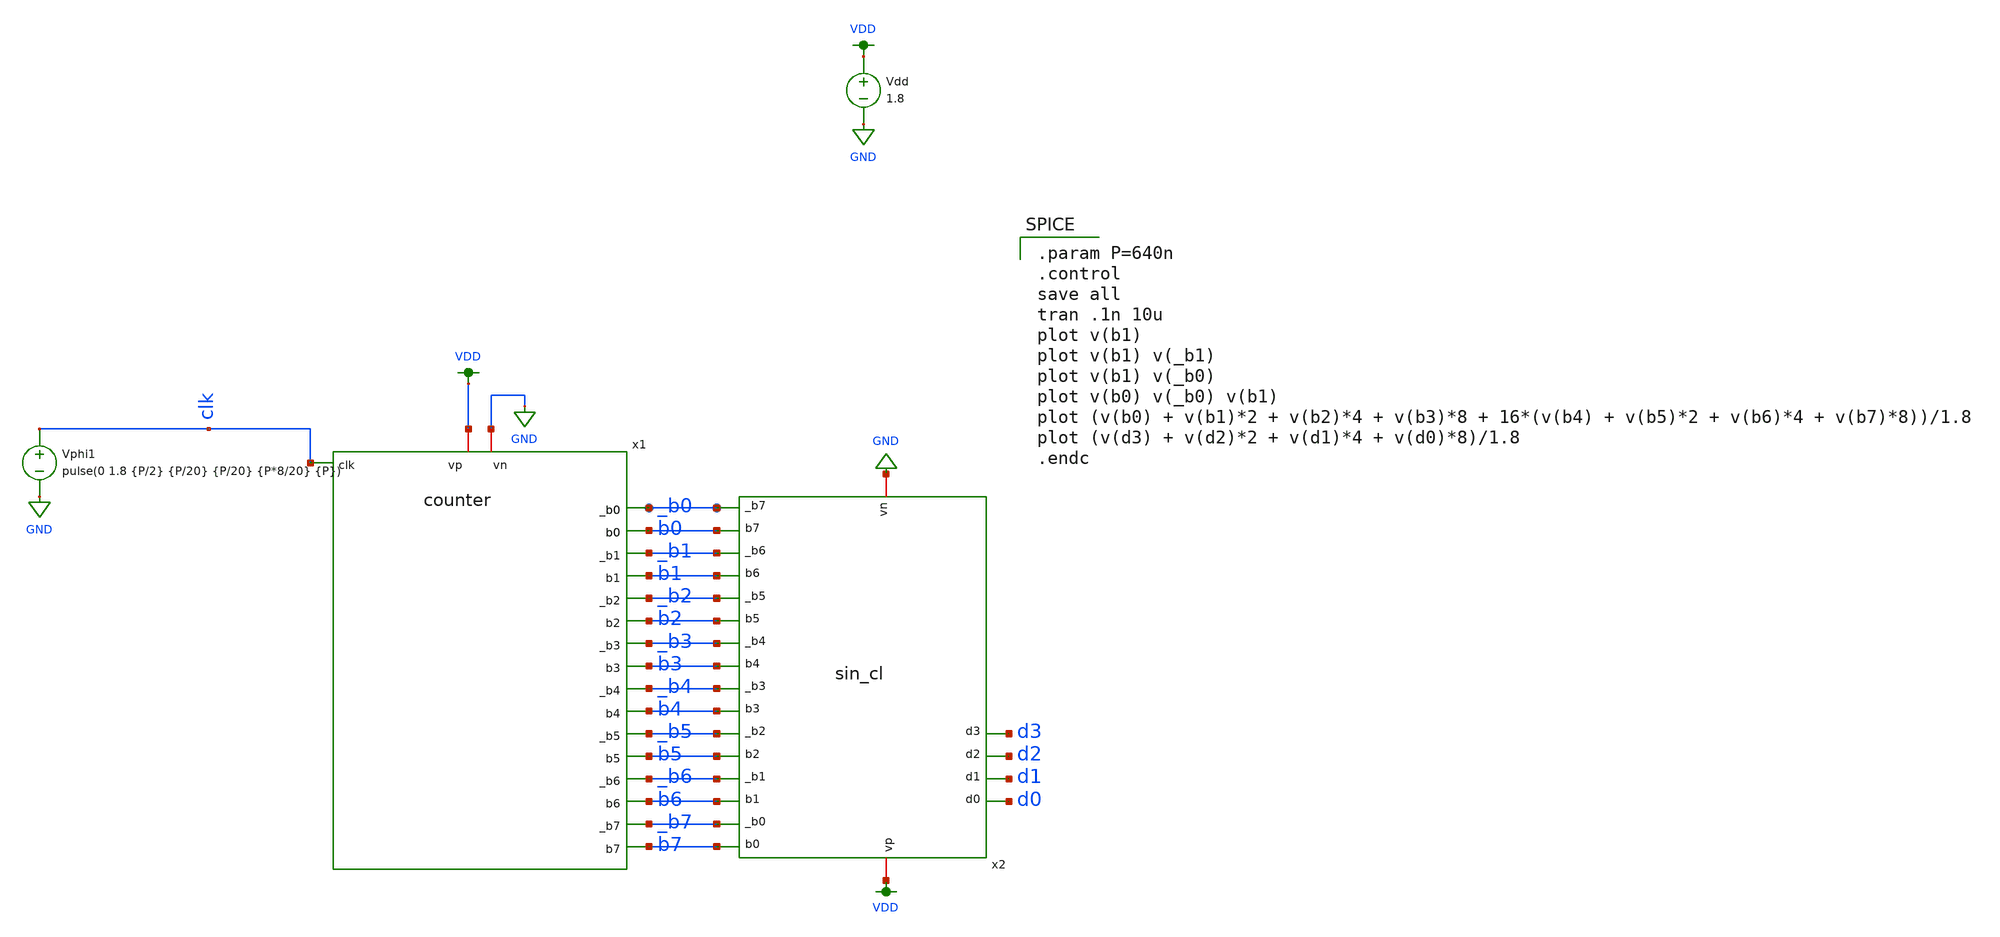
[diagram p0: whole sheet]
** sch_path: xschem/counter_testbench.sch
**.subckt counter_testbench
Vdd VDD GND 1.8
x1 VDD GND clk _b1 b1 _b2 b2 _b3 b3 _b0 b0 _b5 b5 _b6 b6 _b7 b7 _b4 b4 counter
x2 b6 _b6 b5 _b5 b4 _b4 b3 VDD _b3 GND b2 _b2 b1 _b1 d0 b7 b0 _b7 _b0 d1 d2 d3 sin_cl
Vphi1 clk GND pulse(0 1.8 {P/2} {P/20} {P/20} {P*8/20} {P})
**** begin user architecture code

.option wnflag=1
.param MC_SWITCH=0.0
.lib ~/skywater/skywater-pdk/libraries/sky130_fd_pr_ngspice/latest/models/sky130.lib.spice tt


.param P=640n
.control
save all
tran .1n 10u
plot v(b1)
plot v(b1) v(_b1)
plot v(b1) v(_b0)
plot v(b0) v(_b0) v(b1)
plot (v(b0) + v(b1)*2 + v(b2)*4 + v(b3)*8 + 16*(v(b4) + v(b5)*2 + v(b6)*4 + v(b7)*8))/1.8
plot (v(d3) + v(d2)*2 + v(d1)*4 + v(d0)*8)/1.8
.endc

**** end user architecture code
**.ends

* expanding   symbol:  /home/madvlsi/dev/git/magic-dds/xschem/logic_gates/counter.sym # of pins=19
** sym_path: xschem/logic_gates/counter.sym
** sch_path: xschem/logic_gates/counter.sch
.subckt counter vp vn clk _b1 b1 _b2 b2 _b3 b3 _b0 b0 _b5 b5 _b6 b6 _b7 b7 _b4 b4
*.iopin vp
*.iopin vn
*.ipin clk
*.opin b0
*.opin _b0
*.opin b1
*.opin _b1
*.opin b2
*.opin _b2
*.opin b3
*.opin _b3
*.opin b4
*.opin _b4
*.opin b5
*.opin _b5
*.opin b6
*.opin _b6
*.opin b7
*.opin _b7
X1 net2 net1 _b0 b0 clk vp vn dflipflop
x3 vp net2 b0 vn inverter
x2 vp net1 _b0 vn inverter
X4 net4 net3 _b1 b1 _b0 vp vn dflipflop
x5 vp net4 b1 vn inverter
x6 vp net3 _b1 vn inverter
X7 net6 net5 _b2 b2 _b1 vp vn dflipflop
x8 vp net6 b2 vn inverter
x9 vp net5 _b2 vn inverter
X10 net8 net7 _b3 b3 _b2 vp vn dflipflop
x11 vp net8 b3 vn inverter
x12 vp net7 _b3 vn inverter
X13 net10 net9 _b4 b4 _b3 vp vn dflipflop
x14 vp net10 b4 vn inverter
x15 vp net9 _b4 vn inverter
X16 net12 net11 _b5 b5 _b4 vp vn dflipflop
x17 vp net12 b5 vn inverter
x18 vp net11 _b5 vn inverter
X19 net14 net13 _b6 b6 _b5 vp vn dflipflop
x20 vp net14 b6 vn inverter
x21 vp net13 _b6 vn inverter
X22 net16 net15 _b7 b7 _b6 vp vn dflipflop
x23 vp net16 b7 vn inverter
x24 vp net15 _b7 vn inverter
.ends


* expanding   symbol:  /home/madvlsi/dev/git/magic-dds/xschem/sin_cl.sym # of pins=22
** sym_path: xschem/sin_cl.sym
** sch_path: xschem/sin_cl.sch
.subckt sin_cl b1 _b1 b2 _b2 b3 _b3 b4 vp _b4 vn b5 _b5 b6 _b6 d0 b0 b7 _b0 _b7 d1 d2 d3
*.ipin _b0
*.ipin b1
*.ipin _b1
*.ipin b2
*.ipin _b2
*.ipin b3
*.ipin _b3
*.ipin b4
*.ipin _b4
*.ipin b5
*.ipin _b5
*.ipin b6
*.ipin _b6
*.ipin b7
*.ipin _b7
*.ipin b0
*.opin d0
*.opin d1
*.opin d2
*.opin d3
*.iopin vp
*.iopin vn
x1 vp b0 d0 vn inverter
x2 vp _b0 net2 d1 b0 net1 vn xnor
x3 vp net2 net1 vn inverter
x4 vn b1 _b2 net3 vp nand
x5 vn _b1 b2 net4 vp nand
x6 vn _b1 b3 net5 vp b4 nand3
x7 vn b2 _b3 net6 vp _b4 nand3
x8 vn _b1 b4 net7 vp b5 b6 nand4
x9 vn net3 net4 net2 vp net5 net6 net7 nand5
x10 vp _b0 net9 d2 b0 net8 vn xnor
x11 vp net9 net8 vn inverter
x12 vn b1 _b3 net13 vp b4 nand3
x13 vn _b1 b2 net10 vp b4 nand3
x14 vn _b1 b2 net11 vp b5 nand3
x15 vn _b3 b4 net12 vp b5 nand3
x16 vn b1 _b2 net16 vp _b4 nand3
x17 vn b1 _b2 net15 vp _b4 nand3
x18 vn b3 _b4 net14 vp _b5 nand3
x19 vn b3 _b4 net17 vp _b6 nand3
x20 vn net13 net10 net39 vp net11 net12 nand4
x21 vn net16 net15 net40 vp net14 net17 nand4
x22 vp net40 net19 vn inverter
x23 vp net39 net18 vn inverter
x24 vn net18 net19 net9 vp nand
x25 vn _b1 b2 net22 vp b3 nand3
x26 vn b1 b2 net21 vp _b3 b4 nand4
x27 vn b1 _b2 net20 vp b3 b4 nand4
x28 vn b1 b4 net23 vp _b5 _b6 nand4
x29 vn b2 b3 net24 vp _b4 b5 b6 nand5
x30 vn b2 _b3 net27 vp b4 b5 b6 nand5
x31 vn _b2 b3 net26 vp b4 b5 b6 nand5
x32 vn b1 _b2 net25 vp _b3 _b6 nand4
x33 vn b1 _b2 net28 vp _b3 _b4 nand4
x34 vn b1 _b3 net29 vp _b5 _b6 nand4
x35 vn _b1 b2 net32 vp _b4 _b5 nand4
x36 vn _b1 b3 net31 vp _b4 _b5 nand4
x37 vn _b1 b3 net30 vp _b4 _b6 nand4
x38 vn _b2 _b3 net33 vp b4 b5 nand4
x39 vn _b2 _b3 net34 vp _b4 b5 b6 nand5
x40 vn net22 net21 net41 vp net20 net23 net24 nand5
x41 vn net27 net26 net42 vp net25 net28 net29 nand5
x42 vn net32 net31 net43 vp net30 net33 net34 nand5
x43 vp net41 net35 vn inverter
x44 vp net42 net44 vn inverter
x45 vp net43 net36 vn inverter
x46 vn net35 net44 net37 vp net36 nand3
x47 vp _b0 net37 d3 b0 net38 vn xnor
x48 net45 net37 net38 vn inverter
.ends


* expanding   symbol:  /home/madvlsi/dev/git/magic-dds/xschem/logic_gates/dflipflop.sym # of pins=7
** sym_path: xschem/logic_gates/dflipflop.sym
** sch_path: xschem/logic_gates/dflipflop.sch
.subckt dflipflop q_bar q d d_bar clk vp vn
*.opin q
*.opin q_bar
*.iopin vp
*.iopin vn
*.ipin d_bar
*.ipin d
*.ipin clk
XM8 vp net2 net3 vp sky130_fd_pr__pfet_01v8 L=0.15 W=1 nf=1 ad='int((nf+1)/2) * W/nf * 0.29' as='int((nf+2)/2) * W/nf * 0.29'
+ pd='2*int((nf+1)/2) * (W/nf + 0.29)' ps='2*int((nf+2)/2) * (W/nf + 0.29)' nrd='0.29 / W' nrs='0.29 / W'
+ sa=0 sb=0 sd=0 mult=1 m=1
XM9 vp net3 net2 vp sky130_fd_pr__pfet_01v8 L=0.15 W=1 nf=1 ad='int((nf+1)/2) * W/nf * 0.29' as='int((nf+2)/2) * W/nf * 0.29'
+ pd='2*int((nf+1)/2) * (W/nf + 0.29)' ps='2*int((nf+2)/2) * (W/nf + 0.29)' nrd='0.29 / W' nrs='0.29 / W'
+ sa=0 sb=0 sd=0 mult=1 m=1
XM5 net1 clk vn vn sky130_fd_pr__nfet_01v8 L=0.15 W=1 nf=1 ad='int((nf+1)/2) * W/nf * 0.29' as='int((nf+2)/2) * W/nf * 0.29'
+ pd='2*int((nf+1)/2) * (W/nf + 0.29)' ps='2*int((nf+2)/2) * (W/nf + 0.29)' nrd='0.29 / W' nrs='0.29 / W'
+ sa=0 sb=0 sd=0 mult=1 m=1
XM6 net3 net2 net1 vn sky130_fd_pr__nfet_01v8 L=0.15 W=1 nf=1 ad='int((nf+1)/2) * W/nf * 0.29' as='int((nf+2)/2) * W/nf * 0.29'
+ pd='2*int((nf+1)/2) * (W/nf + 0.29)' ps='2*int((nf+2)/2) * (W/nf + 0.29)' nrd='0.29 / W' nrs='0.29 / W'
+ sa=0 sb=0 sd=0 mult=1 m=1
XM7 net2 net3 net1 vn sky130_fd_pr__nfet_01v8 L=0.15 W=1 nf=1 ad='int((nf+1)/2) * W/nf * 0.29' as='int((nf+2)/2) * W/nf * 0.29'
+ pd='2*int((nf+1)/2) * (W/nf + 0.29)' ps='2*int((nf+2)/2) * (W/nf + 0.29)' nrd='0.29 / W' nrs='0.29 / W'
+ sa=0 sb=0 sd=0 mult=1 m=1
XM13 vn q q_bar vn sky130_fd_pr__nfet_01v8 L=0.15 W=1 nf=1 ad='int((nf+1)/2) * W/nf * 0.29' as='int((nf+2)/2) * W/nf * 0.29'
+ pd='2*int((nf+1)/2) * (W/nf + 0.29)' ps='2*int((nf+2)/2) * (W/nf + 0.29)' nrd='0.29 / W' nrs='0.29 / W'
+ sa=0 sb=0 sd=0 mult=1 m=1
XM3 q clk net2 vn sky130_fd_pr__nfet_01v8 L=0.30 W=1 nf=1 ad='int((nf+1)/2) * W/nf * 0.29' as='int((nf+2)/2) * W/nf * 0.29'
+ pd='2*int((nf+1)/2) * (W/nf + 0.29)' ps='2*int((nf+2)/2) * (W/nf + 0.29)' nrd='0.29 / W' nrs='0.29 / W'
+ sa=0 sb=0 sd=0 mult=1 m=1
XM4 q_bar clk net3 vn sky130_fd_pr__nfet_01v8 L=0.30 W=1 nf=1 ad='int((nf+1)/2) * W/nf * 0.29' as='int((nf+2)/2) * W/nf * 0.29'
+ pd='2*int((nf+1)/2) * (W/nf + 0.29)' ps='2*int((nf+2)/2) * (W/nf + 0.29)' nrd='0.29 / W' nrs='0.29 / W'
+ sa=0 sb=0 sd=0 mult=1 m=1
XM14 vn q_bar q vn sky130_fd_pr__nfet_01v8 L=0.15 W=1 nf=1 ad='int((nf+1)/2) * W/nf * 0.29' as='int((nf+2)/2) * W/nf * 0.29'
+ pd='2*int((nf+1)/2) * (W/nf + 0.29)' ps='2*int((nf+2)/2) * (W/nf + 0.29)' nrd='0.29 / W' nrs='0.29 / W'
+ sa=0 sb=0 sd=0 mult=1 m=1
XM10 net4 clk vp vp sky130_fd_pr__pfet_01v8 L=0.15 W=1 nf=1 ad='int((nf+1)/2) * W/nf * 0.29' as='int((nf+2)/2) * W/nf * 0.29'
+ pd='2*int((nf+1)/2) * (W/nf + 0.29)' ps='2*int((nf+2)/2) * (W/nf + 0.29)' nrd='0.29 / W' nrs='0.29 / W'
+ sa=0 sb=0 sd=0 mult=1 m=1
XM11 q_bar q net4 vp sky130_fd_pr__pfet_01v8 L=0.15 W=1 nf=1 ad='int((nf+1)/2) * W/nf * 0.29' as='int((nf+2)/2) * W/nf * 0.29'
+ pd='2*int((nf+1)/2) * (W/nf + 0.29)' ps='2*int((nf+2)/2) * (W/nf + 0.29)' nrd='0.29 / W' nrs='0.29 / W'
+ sa=0 sb=0 sd=0 mult=1 m=1
XM12 q q_bar net4 vp sky130_fd_pr__pfet_01v8 L=0.15 W=1 nf=1 ad='int((nf+1)/2) * W/nf * 0.29' as='int((nf+2)/2) * W/nf * 0.29'
+ pd='2*int((nf+1)/2) * (W/nf + 0.29)' ps='2*int((nf+2)/2) * (W/nf + 0.29)' nrd='0.29 / W' nrs='0.29 / W'
+ sa=0 sb=0 sd=0 mult=1 m=1
XM15 net1 clk vn vn sky130_fd_pr__nfet_01v8 L=0.15 W=1 nf=1 ad='int((nf+1)/2) * W/nf * 0.29' as='int((nf+2)/2) * W/nf * 0.29'
+ pd='2*int((nf+1)/2) * (W/nf + 0.29)' ps='2*int((nf+2)/2) * (W/nf + 0.29)' nrd='0.29 / W' nrs='0.29 / W'
+ sa=0 sb=0 sd=0 mult=1 m=1
XM16 net4 clk vp vp sky130_fd_pr__pfet_01v8 L=0.15 W=1 nf=1 ad='int((nf+1)/2) * W/nf * 0.29' as='int((nf+2)/2) * W/nf * 0.29'
+ pd='2*int((nf+1)/2) * (W/nf + 0.29)' ps='2*int((nf+2)/2) * (W/nf + 0.29)' nrd='0.29 / W' nrs='0.29 / W'
+ sa=0 sb=0 sd=0 mult=1 m=1
XM1 net2 clk d vp sky130_fd_pr__pfet_01v8 L=0.30 W=1 nf=1 ad='int((nf+1)/2) * W/nf * 0.29' as='int((nf+2)/2) * W/nf * 0.29'
+ pd='2*int((nf+1)/2) * (W/nf + 0.29)' ps='2*int((nf+2)/2) * (W/nf + 0.29)' nrd='0.29 / W' nrs='0.29 / W'
+ sa=0 sb=0 sd=0 mult=1 m=1
XM2 net3 clk d_bar vp sky130_fd_pr__pfet_01v8 L=0.30 W=1 nf=1 ad='int((nf+1)/2) * W/nf * 0.29' as='int((nf+2)/2) * W/nf * 0.29'
+ pd='2*int((nf+1)/2) * (W/nf + 0.29)' ps='2*int((nf+2)/2) * (W/nf + 0.29)' nrd='0.29 / W' nrs='0.29 / W'
+ sa=0 sb=0 sd=0 mult=1 m=1
.ends


* expanding   symbol:  /home/madvlsi/dev/git/magic-dds/xschem/other_project_files/inverter.sym # of
*+ pins=4
** sym_path: xschem/other_project_files/inverter.sym
** sch_path: xschem/other_project_files/inverter.sch
.subckt inverter VP A Y VN
*.iopin VP
*.iopin VN
*.ipin A
*.opin Y
XM1 Y A VN VN sky130_fd_pr__nfet_01v8 L=0.15 W=1 nf=1 ad='int((nf+1)/2) * W/nf * 0.29' as='int((nf+2)/2) * W/nf * 0.29'
+ pd='2*int((nf+1)/2) * (W/nf + 0.29)' ps='2*int((nf+2)/2) * (W/nf + 0.29)' nrd='0.29 / W' nrs='0.29 / W'
+ sa=0 sb=0 sd=0 mult=1 m=1
XM2 Y A VP VP sky130_fd_pr__pfet_01v8 L=0.15 W=4 nf=1 ad='int((nf+1)/2) * W/nf * 0.29' as='int((nf+2)/2) * W/nf * 0.29'
+ pd='2*int((nf+1)/2) * (W/nf + 0.29)' ps='2*int((nf+2)/2) * (W/nf + 0.29)' nrd='0.29 / W' nrs='0.29 / W'
+ sa=0 sb=0 sd=0 mult=1 m=1
.ends


* expanding   symbol:  /home/madvlsi/dev/git/magic-dds/xschem/logic_gates/xnor.sym # of pins=7
** sym_path: xschem/logic_gates/xnor.sym
** sch_path: xschem/logic_gates/xnor.sch
.subckt xnor vp A B Y _A _B vn
*.iopin vp
*.iopin vn
*.ipin A
*.ipin B
*.ipin _A
*.ipin _B
*.opin Y
x1 vn A B net1 vp nand
x2 vn _A _B net2 vp nand
x3 vn net1 net2 Y vp nand
.ends


* expanding   symbol:  /home/madvlsi/dev/git/magic-dds/xschem/logic_gates/nand.sym # of pins=5
** sym_path: xschem/logic_gates/nand.sym
** sch_path: xschem/logic_gates/nand.sch
.subckt nand VN A B Y VP
*.iopin VP
*.iopin VN
*.ipin A
*.ipin B
*.opin Y
XM1 Y A net1 GND sky130_fd_pr__nfet_01v8 L=0.15 W=1 nf=1 ad='int((nf+1)/2) * W/nf * 0.29' as='int((nf+2)/2) * W/nf * 0.29'
+ pd='2*int((nf+1)/2) * (W/nf + 0.29)' ps='2*int((nf+2)/2) * (W/nf + 0.29)' nrd='0.29 / W' nrs='0.29 / W'
+ sa=0 sb=0 sd=0 mult=1 m=1
XM2 net1 B VN GND sky130_fd_pr__nfet_01v8 L=0.15 W=1 nf=1 ad='int((nf+1)/2) * W/nf * 0.29' as='int((nf+2)/2) * W/nf * 0.29'
+ pd='2*int((nf+1)/2) * (W/nf + 0.29)' ps='2*int((nf+2)/2) * (W/nf + 0.29)' nrd='0.29 / W' nrs='0.29 / W'
+ sa=0 sb=0 sd=0 mult=1 m=1
XM3 Y A VP VDD sky130_fd_pr__pfet_01v8 L=0.15 W=1 nf=1 ad='int((nf+1)/2) * W/nf * 0.29' as='int((nf+2)/2) * W/nf * 0.29'
+ pd='2*int((nf+1)/2) * (W/nf + 0.29)' ps='2*int((nf+2)/2) * (W/nf + 0.29)' nrd='0.29 / W' nrs='0.29 / W'
+ sa=0 sb=0 sd=0 mult=1 m=1
XM4 Y B VP VDD sky130_fd_pr__pfet_01v8 L=0.15 W=1 nf=1 ad='int((nf+1)/2) * W/nf * 0.29' as='int((nf+2)/2) * W/nf * 0.29'
+ pd='2*int((nf+1)/2) * (W/nf + 0.29)' ps='2*int((nf+2)/2) * (W/nf + 0.29)' nrd='0.29 / W' nrs='0.29 / W'
+ sa=0 sb=0 sd=0 mult=1 m=1
.ends


* expanding   symbol:  /home/madvlsi/dev/git/magic-dds/xschem/logic_gates/nand3.sym # of pins=6
** sym_path: xschem/logic_gates/nand3.sym
** sch_path: xschem/logic_gates/nand3.sch
.subckt nand3 VN A B Y VP C
*.iopin VP
*.iopin VN
*.ipin A
*.ipin B
*.opin Y
*.ipin C
XM1 Y A net1 GND sky130_fd_pr__nfet_01v8 L=0.15 W=1 nf=1 ad='int((nf+1)/2) * W/nf * 0.29' as='int((nf+2)/2) * W/nf * 0.29'
+ pd='2*int((nf+1)/2) * (W/nf + 0.29)' ps='2*int((nf+2)/2) * (W/nf + 0.29)' nrd='0.29 / W' nrs='0.29 / W'
+ sa=0 sb=0 sd=0 mult=1 m=1
XM2 net1 B net2 GND sky130_fd_pr__nfet_01v8 L=0.15 W=1 nf=1 ad='int((nf+1)/2) * W/nf * 0.29' as='int((nf+2)/2) * W/nf * 0.29'
+ pd='2*int((nf+1)/2) * (W/nf + 0.29)' ps='2*int((nf+2)/2) * (W/nf + 0.29)' nrd='0.29 / W' nrs='0.29 / W'
+ sa=0 sb=0 sd=0 mult=1 m=1
XM3 Y A VP VDD sky130_fd_pr__pfet_01v8 L=0.15 W=1 nf=1 ad='int((nf+1)/2) * W/nf * 0.29' as='int((nf+2)/2) * W/nf * 0.29'
+ pd='2*int((nf+1)/2) * (W/nf + 0.29)' ps='2*int((nf+2)/2) * (W/nf + 0.29)' nrd='0.29 / W' nrs='0.29 / W'
+ sa=0 sb=0 sd=0 mult=1 m=1
XM4 Y B VP VDD sky130_fd_pr__pfet_01v8 L=0.15 W=1 nf=1 ad='int((nf+1)/2) * W/nf * 0.29' as='int((nf+2)/2) * W/nf * 0.29'
+ pd='2*int((nf+1)/2) * (W/nf + 0.29)' ps='2*int((nf+2)/2) * (W/nf + 0.29)' nrd='0.29 / W' nrs='0.29 / W'
+ sa=0 sb=0 sd=0 mult=1 m=1
XM5 net2 C VN GND sky130_fd_pr__nfet_01v8 L=0.15 W=1 nf=1 ad='int((nf+1)/2) * W/nf * 0.29' as='int((nf+2)/2) * W/nf * 0.29'
+ pd='2*int((nf+1)/2) * (W/nf + 0.29)' ps='2*int((nf+2)/2) * (W/nf + 0.29)' nrd='0.29 / W' nrs='0.29 / W'
+ sa=0 sb=0 sd=0 mult=1 m=1
XM6 Y C VP VDD sky130_fd_pr__pfet_01v8 L=0.15 W=1 nf=1 ad='int((nf+1)/2) * W/nf * 0.29' as='int((nf+2)/2) * W/nf * 0.29'
+ pd='2*int((nf+1)/2) * (W/nf + 0.29)' ps='2*int((nf+2)/2) * (W/nf + 0.29)' nrd='0.29 / W' nrs='0.29 / W'
+ sa=0 sb=0 sd=0 mult=1 m=1
.ends


* expanding   symbol:  /home/madvlsi/dev/git/magic-dds/xschem/logic_gates/nand4.sym # of pins=7
** sym_path: xschem/logic_gates/nand4.sym
** sch_path: xschem/logic_gates/nand4.sch
.subckt nand4 VN A B Y VP C D
*.iopin VP
*.iopin VN
*.ipin A
*.ipin B
*.opin Y
*.ipin C
*.ipin D
XM1 Y A net1 GND sky130_fd_pr__nfet_01v8 L=0.15 W=1 nf=1 ad='int((nf+1)/2) * W/nf * 0.29' as='int((nf+2)/2) * W/nf * 0.29'
+ pd='2*int((nf+1)/2) * (W/nf + 0.29)' ps='2*int((nf+2)/2) * (W/nf + 0.29)' nrd='0.29 / W' nrs='0.29 / W'
+ sa=0 sb=0 sd=0 mult=1 m=1
XM2 net1 B net2 GND sky130_fd_pr__nfet_01v8 L=0.15 W=1 nf=1 ad='int((nf+1)/2) * W/nf * 0.29' as='int((nf+2)/2) * W/nf * 0.29'
+ pd='2*int((nf+1)/2) * (W/nf + 0.29)' ps='2*int((nf+2)/2) * (W/nf + 0.29)' nrd='0.29 / W' nrs='0.29 / W'
+ sa=0 sb=0 sd=0 mult=1 m=1
XM3 Y A VP VDD sky130_fd_pr__pfet_01v8 L=0.15 W=1 nf=1 ad='int((nf+1)/2) * W/nf * 0.29' as='int((nf+2)/2) * W/nf * 0.29'
+ pd='2*int((nf+1)/2) * (W/nf + 0.29)' ps='2*int((nf+2)/2) * (W/nf + 0.29)' nrd='0.29 / W' nrs='0.29 / W'
+ sa=0 sb=0 sd=0 mult=1 m=1
XM4 Y B VP VDD sky130_fd_pr__pfet_01v8 L=0.15 W=1 nf=1 ad='int((nf+1)/2) * W/nf * 0.29' as='int((nf+2)/2) * W/nf * 0.29'
+ pd='2*int((nf+1)/2) * (W/nf + 0.29)' ps='2*int((nf+2)/2) * (W/nf + 0.29)' nrd='0.29 / W' nrs='0.29 / W'
+ sa=0 sb=0 sd=0 mult=1 m=1
XM5 net2 C net3 GND sky130_fd_pr__nfet_01v8 L=0.15 W=1 nf=1 ad='int((nf+1)/2) * W/nf * 0.29' as='int((nf+2)/2) * W/nf * 0.29'
+ pd='2*int((nf+1)/2) * (W/nf + 0.29)' ps='2*int((nf+2)/2) * (W/nf + 0.29)' nrd='0.29 / W' nrs='0.29 / W'
+ sa=0 sb=0 sd=0 mult=1 m=1
XM6 Y C VP VDD sky130_fd_pr__pfet_01v8 L=0.15 W=1 nf=1 ad='int((nf+1)/2) * W/nf * 0.29' as='int((nf+2)/2) * W/nf * 0.29'
+ pd='2*int((nf+1)/2) * (W/nf + 0.29)' ps='2*int((nf+2)/2) * (W/nf + 0.29)' nrd='0.29 / W' nrs='0.29 / W'
+ sa=0 sb=0 sd=0 mult=1 m=1
XM7 Y D VP VDD sky130_fd_pr__pfet_01v8 L=0.15 W=1 nf=1 ad='int((nf+1)/2) * W/nf * 0.29' as='int((nf+2)/2) * W/nf * 0.29'
+ pd='2*int((nf+1)/2) * (W/nf + 0.29)' ps='2*int((nf+2)/2) * (W/nf + 0.29)' nrd='0.29 / W' nrs='0.29 / W'
+ sa=0 sb=0 sd=0 mult=1 m=1
XM8 net3 D VN GND sky130_fd_pr__nfet_01v8 L=0.15 W=1 nf=1 ad='int((nf+1)/2) * W/nf * 0.29' as='int((nf+2)/2) * W/nf * 0.29'
+ pd='2*int((nf+1)/2) * (W/nf + 0.29)' ps='2*int((nf+2)/2) * (W/nf + 0.29)' nrd='0.29 / W' nrs='0.29 / W'
+ sa=0 sb=0 sd=0 mult=1 m=1
.ends


* expanding   symbol:  /home/madvlsi/dev/git/magic-dds/xschem/logic_gates/nand5.sym # of pins=8
** sym_path: xschem/logic_gates/nand5.sym
** sch_path: xschem/logic_gates/nand5.sch
.subckt nand5 VN A B Y VP C D E
*.iopin VP
*.iopin VN
*.ipin A
*.ipin B
*.opin Y
*.ipin C
*.ipin D
*.ipin E
XM1 Y A net1 GND sky130_fd_pr__nfet_01v8 L=0.15 W=1 nf=1 ad='int((nf+1)/2) * W/nf * 0.29' as='int((nf+2)/2) * W/nf * 0.29'
+ pd='2*int((nf+1)/2) * (W/nf + 0.29)' ps='2*int((nf+2)/2) * (W/nf + 0.29)' nrd='0.29 / W' nrs='0.29 / W'
+ sa=0 sb=0 sd=0 mult=1 m=1
XM2 net1 B net2 GND sky130_fd_pr__nfet_01v8 L=0.15 W=1 nf=1 ad='int((nf+1)/2) * W/nf * 0.29' as='int((nf+2)/2) * W/nf * 0.29'
+ pd='2*int((nf+1)/2) * (W/nf + 0.29)' ps='2*int((nf+2)/2) * (W/nf + 0.29)' nrd='0.29 / W' nrs='0.29 / W'
+ sa=0 sb=0 sd=0 mult=1 m=1
XM3 Y A VP VDD sky130_fd_pr__pfet_01v8 L=0.15 W=1 nf=1 ad='int((nf+1)/2) * W/nf * 0.29' as='int((nf+2)/2) * W/nf * 0.29'
+ pd='2*int((nf+1)/2) * (W/nf + 0.29)' ps='2*int((nf+2)/2) * (W/nf + 0.29)' nrd='0.29 / W' nrs='0.29 / W'
+ sa=0 sb=0 sd=0 mult=1 m=1
XM4 Y B VP VDD sky130_fd_pr__pfet_01v8 L=0.15 W=1 nf=1 ad='int((nf+1)/2) * W/nf * 0.29' as='int((nf+2)/2) * W/nf * 0.29'
+ pd='2*int((nf+1)/2) * (W/nf + 0.29)' ps='2*int((nf+2)/2) * (W/nf + 0.29)' nrd='0.29 / W' nrs='0.29 / W'
+ sa=0 sb=0 sd=0 mult=1 m=1
XM5 net2 C net3 GND sky130_fd_pr__nfet_01v8 L=0.15 W=1 nf=1 ad='int((nf+1)/2) * W/nf * 0.29' as='int((nf+2)/2) * W/nf * 0.29'
+ pd='2*int((nf+1)/2) * (W/nf + 0.29)' ps='2*int((nf+2)/2) * (W/nf + 0.29)' nrd='0.29 / W' nrs='0.29 / W'
+ sa=0 sb=0 sd=0 mult=1 m=1
XM6 Y C VP VDD sky130_fd_pr__pfet_01v8 L=0.15 W=1 nf=1 ad='int((nf+1)/2) * W/nf * 0.29' as='int((nf+2)/2) * W/nf * 0.29'
+ pd='2*int((nf+1)/2) * (W/nf + 0.29)' ps='2*int((nf+2)/2) * (W/nf + 0.29)' nrd='0.29 / W' nrs='0.29 / W'
+ sa=0 sb=0 sd=0 mult=1 m=1
XM7 Y D VP VDD sky130_fd_pr__pfet_01v8 L=0.15 W=1 nf=1 ad='int((nf+1)/2) * W/nf * 0.29' as='int((nf+2)/2) * W/nf * 0.29'
+ pd='2*int((nf+1)/2) * (W/nf + 0.29)' ps='2*int((nf+2)/2) * (W/nf + 0.29)' nrd='0.29 / W' nrs='0.29 / W'
+ sa=0 sb=0 sd=0 mult=1 m=1
XM8 net3 D net4 GND sky130_fd_pr__nfet_01v8 L=0.15 W=1 nf=1 ad='int((nf+1)/2) * W/nf * 0.29' as='int((nf+2)/2) * W/nf * 0.29'
+ pd='2*int((nf+1)/2) * (W/nf + 0.29)' ps='2*int((nf+2)/2) * (W/nf + 0.29)' nrd='0.29 / W' nrs='0.29 / W'
+ sa=0 sb=0 sd=0 mult=1 m=1
XM9 Y E VP VDD sky130_fd_pr__pfet_01v8 L=0.15 W=1 nf=1 ad='int((nf+1)/2) * W/nf * 0.29' as='int((nf+2)/2) * W/nf * 0.29'
+ pd='2*int((nf+1)/2) * (W/nf + 0.29)' ps='2*int((nf+2)/2) * (W/nf + 0.29)' nrd='0.29 / W' nrs='0.29 / W'
+ sa=0 sb=0 sd=0 mult=1 m=1
XM10 net4 E VN GND sky130_fd_pr__nfet_01v8 L=0.15 W=1 nf=1 ad='int((nf+1)/2) * W/nf * 0.29' as='int((nf+2)/2) * W/nf * 0.29'
+ pd='2*int((nf+1)/2) * (W/nf + 0.29)' ps='2*int((nf+2)/2) * (W/nf + 0.29)' nrd='0.29 / W' nrs='0.29 / W'
+ sa=0 sb=0 sd=0 mult=1 m=1
.ends

.GLOBAL VDD
.GLOBAL GND
.end
